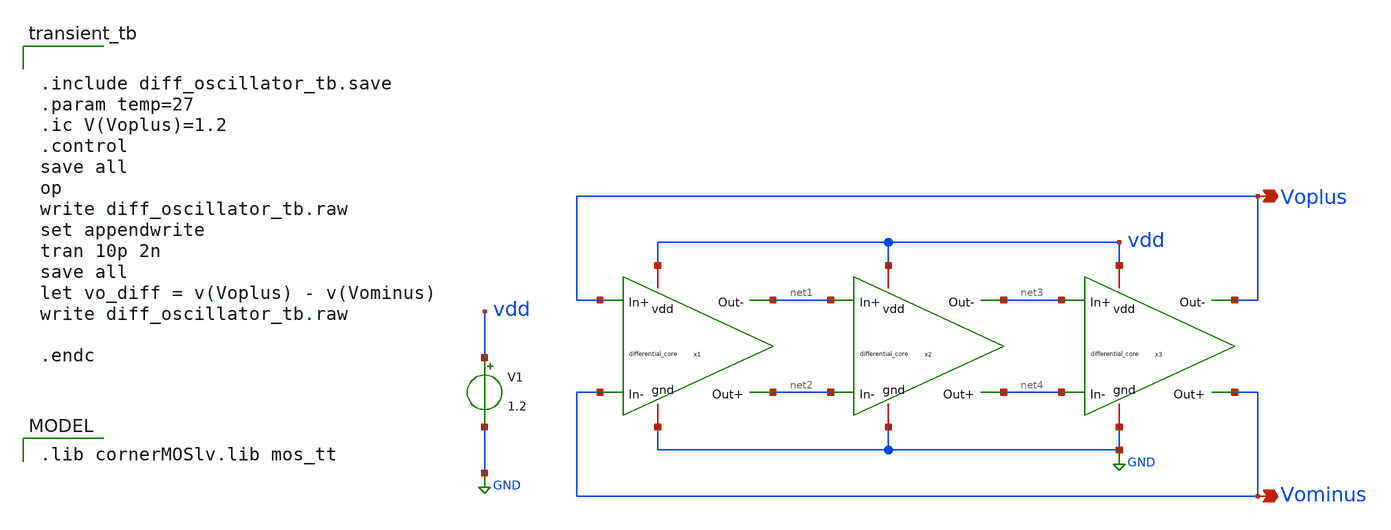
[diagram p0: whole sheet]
** sch_path: modules/module_4_type_2_PLL/diff_Roscillator/testbench/diff_oscillator_tb.sch
**.subckt diff_oscillator_tb Voplus Vominus
*.opin Voplus
*.opin Vominus
x1 vdd net2 net1 Voplus Vominus GND differential_core
x2 vdd net4 net3 net1 net2 GND differential_core
x3 vdd Vominus Voplus net3 net4 GND differential_core
V1 vdd GND 1.2
**** begin user architecture code


.include diff_oscillator_tb.save
.param temp=27
.ic V(Voplus)=1.2
.control
save all
op
write diff_oscillator_tb.raw
set appendwrite
tran 10p 2n
save all
let vo_diff = v(Voplus) - v(Vominus)
write diff_oscillator_tb.raw

.endc


 .lib cornerMOSlv.lib mos_tt

**** end user architecture code
**.ends

* expanding   symbol:  differential_core.sym # of pins=6
** sym_path: modules/module_4_type_2_PLL/diff_Roscillator/schematic/differential_core.sym
** sch_path: modules/module_4_type_2_PLL/diff_Roscillator/schematic/differential_core.sch
.subckt differential_core vdd Out+ Out- In+ In- gnd
*.ipin In+
*.iopin vdd
*.iopin gnd
*.ipin In-
*.opin Out+
*.opin Out-
XM1 Out+ In- net1 gnd sg13_lv_nmos w=2.6u l=0.26u ng=1 m=1 mm_ok=1
XM2 Out- In+ net1 gnd sg13_lv_nmos w=2.6u l=0.26u ng=1 m=1 mm_ok=1
R1 vdd Out- 5k m=1
R2 vdd Out+ 5k m=1
C1 Out- gnd 0.5f m=1
C2 Out+ gnd 0.5f m=1
I0 net1 gnd 200u
.ends

.GLOBAL GND
.end
